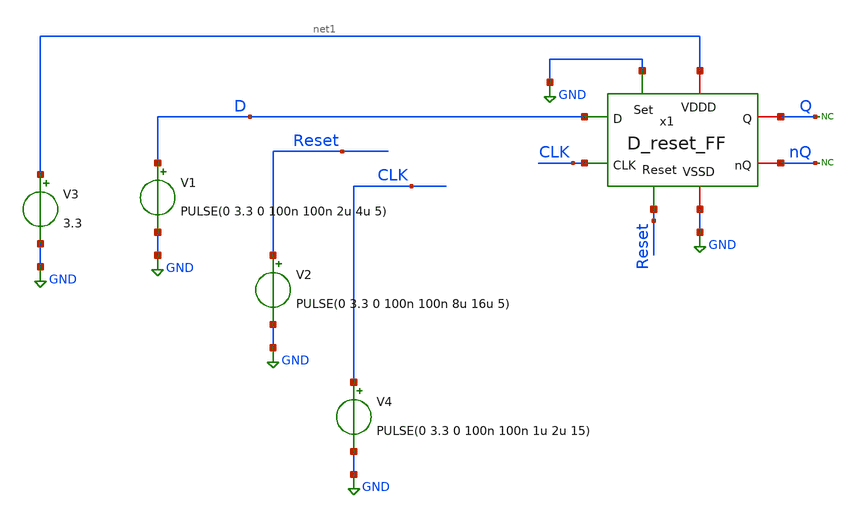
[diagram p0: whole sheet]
** sch_path: SAR_ADC/blocks/SAR_logic/D_reset_FF_tb.sch
**.subckt D_reset_FF_tb
x1 net1 Q CLK D nQ GND Reset GND D_reset_FF
* noconn Q
* noconn nQ
V3 net1 GND 3.3
V1 D GND PULSE(0 3.3 0 100n 100n 2u 4u 5)
V2 Reset GND PULSE(0 3.3 0 100n 100n 8u 16u 5)
V4 CLK GND PULSE(0 3.3 0 100n 100n 1u 2u 15)
**** begin user architecture code



*Parameters
.options TEMPS= 27.0

*Models
.include /home/electrica/Documents/gf180_projects/pdk/gf180mcuC/libs.tech/ngspice/design.ngspice
.lib /home/electrica/Documents/gf180_projects/pdk/gf180mcuC/libs.tech/ngspice/sm141064.ngspice typical
.lib /home/electrica/Documents/gf180_projects/pdk/gf180mcuC/libs.tech/ngspice/smbb000149.ngspice typical


*Data to save
.save all

*Simulation
.control
tran 1n 30u
setplot dc1
plot V(D)+4 V(Reset)+8 V(CLK)+12 V(Q)
set filetype=ascii
write D_reset_FF_tb_tran.raw

reset
unset filetype
op
save all
write D_reset_FF_tb.raw

.endc
.end



**** end user architecture code
**.ends
.GLOBAL GND
.end
